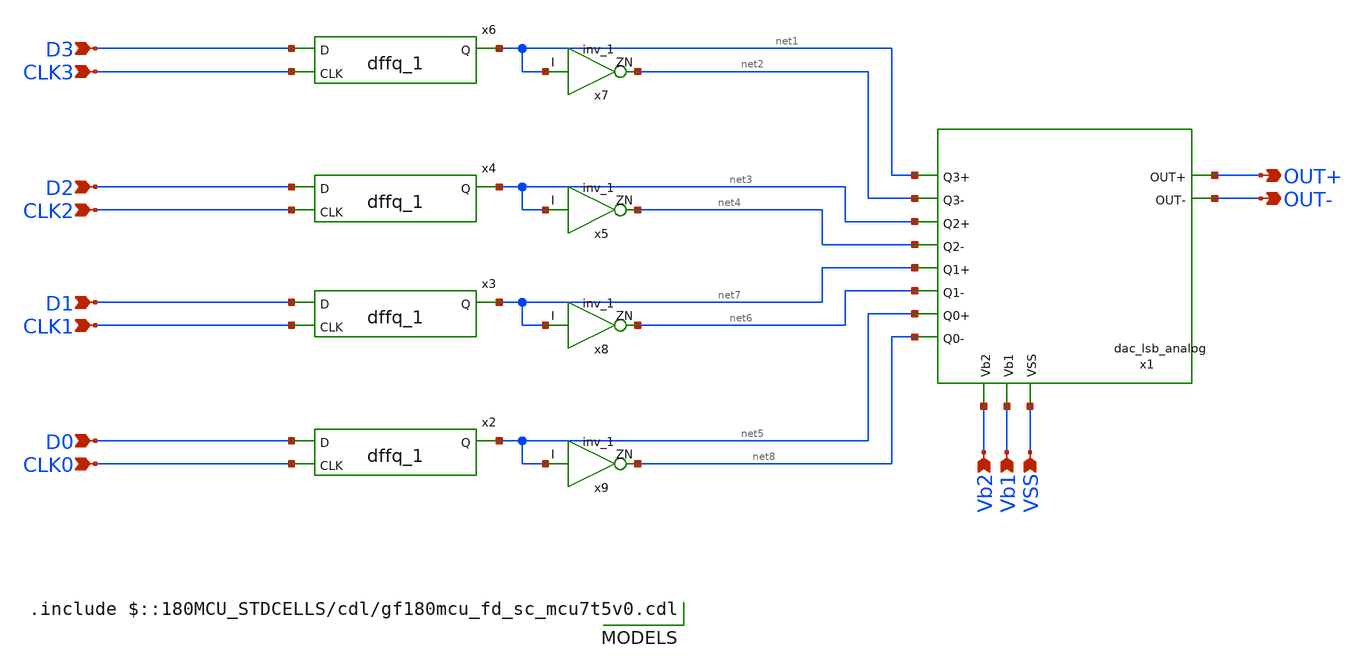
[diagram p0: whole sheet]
** sch_path: DAC/xschem/dac_lsb_matrix.sch
**.subckt dac_lsb_matrix D3 D2 D1 D0 CLK3 CLK2 CLK1 CLK0 VSS Vb2 Vb1 OUT+ OUT-
*.ipin D3
*.ipin D2
*.ipin D1
*.ipin D0
*.ipin CLK3
*.ipin CLK2
*.ipin CLK1
*.ipin CLK0
*.ipin VSS
*.ipin Vb2
*.ipin Vb1
*.opin OUT+
*.opin OUT-
x1 OUT+ OUT- net4 net1 net6 net3 net2 net7 net8 net5 Vb2 Vb1 VSS dac_lsb_analog
x6 D3 CLK3 net1 DVDD DVDD DVSS DVSS gf180mcu_fd_sc_mcu7t5v0__dffq_1
x7 net1 net2 DVDD DVDD DVSS DVSS gf180mcu_fd_sc_mcu7t5v0__inv_1
x4 D2 CLK2 net3 DVDD DVDD DVSS DVSS gf180mcu_fd_sc_mcu7t5v0__dffq_1
x5 net3 net4 DVDD DVDD DVSS DVSS gf180mcu_fd_sc_mcu7t5v0__inv_1
x3 D1 CLK1 net7 DVDD DVDD DVSS DVSS gf180mcu_fd_sc_mcu7t5v0__dffq_1
x8 net7 net6 DVDD DVDD DVSS DVSS gf180mcu_fd_sc_mcu7t5v0__inv_1
x2 D0 CLK0 net5 DVDD DVDD DVSS DVSS gf180mcu_fd_sc_mcu7t5v0__dffq_1
x9 net5 net8 DVDD DVDD DVSS DVSS gf180mcu_fd_sc_mcu7t5v0__inv_1
**** begin user architecture code

.include $::180MCU_STDCELLS/cdl/gf180mcu_fd_sc_mcu7t5v0.cdl

**** end user architecture code
**.ends

* expanding   symbol:  dac_lsb_analog.sym # of pins=13
** sym_path: DAC/xschem/dac_lsb_analog.sym
** sch_path: DAC/xschem/dac_lsb_analog.sch
.subckt dac_lsb_analog OUT+ OUT- Q2- Q3+ Q1- Q2+ Q3- Q1+ Q0- Q0+ Vb2 Vb1 VSS
*.ipin VSS
*.ipin Vb2
*.ipin Vb1
*.ipin Q3-
*.ipin Q3+
*.ipin Q2-
*.ipin Q2+
*.ipin Q1-
*.ipin Q1+
*.ipin Q0-
*.ipin Q0+
*.opin OUT+
*.opin OUT-
XM7 net1 Vb2 net2 VSS nfet_03v3 L=0.5u W=2u nf=2 ad='int((nf+1)/2) * W/nf * 0.18u' as='int((nf+2)/2) * W/nf * 0.18u'
+ pd='2*int((nf+1)/2) * (W/nf + 0.18u)' ps='2*int((nf+2)/2) * (W/nf + 0.18u)' nrd='0.18u / W' nrs='0.18u / W'
+ sa=0 sb=0 sd=0 m=1
XM8 net2 Vb1 VSS VSS nfet_03v3 L=0.5u W=2u nf=1 ad='int((nf+1)/2) * W/nf * 0.18u' as='int((nf+2)/2) * W/nf * 0.18u'
+ pd='2*int((nf+1)/2) * (W/nf + 0.18u)' ps='2*int((nf+2)/2) * (W/nf + 0.18u)' nrd='0.18u / W' nrs='0.18u / W'
+ sa=0 sb=0 sd=0 m=1
XM12 OUT+ Q0+ net1 VSS nfet_03v3 L=0.5u W=1u nf=1 ad='int((nf+1)/2) * W/nf * 0.18u' as='int((nf+2)/2) * W/nf * 0.18u'
+ pd='2*int((nf+1)/2) * (W/nf + 0.18u)' ps='2*int((nf+2)/2) * (W/nf + 0.18u)' nrd='0.18u / W' nrs='0.18u / W'
+ sa=0 sb=0 sd=0 m=1
XM13 OUT- Q0- net1 VSS nfet_03v3 L=0.5u W=1u nf=1 ad='int((nf+1)/2) * W/nf * 0.18u' as='int((nf+2)/2) * W/nf * 0.18u'
+ pd='2*int((nf+1)/2) * (W/nf + 0.18u)' ps='2*int((nf+2)/2) * (W/nf + 0.18u)' nrd='0.18u / W' nrs='0.18u / W'
+ sa=0 sb=0 sd=0 m=1
XM14 net3 Vb2 net4 VSS nfet_03v3 L=0.5u W=4u nf=4 ad='int((nf+1)/2) * W/nf * 0.18u' as='int((nf+2)/2) * W/nf * 0.18u'
+ pd='2*int((nf+1)/2) * (W/nf + 0.18u)' ps='2*int((nf+2)/2) * (W/nf + 0.18u)' nrd='0.18u / W' nrs='0.18u / W'
+ sa=0 sb=0 sd=0 m=1
XM15 net4 Vb1 VSS VSS nfet_03v3 L=0.5u W=4u nf=2 ad='int((nf+1)/2) * W/nf * 0.18u' as='int((nf+2)/2) * W/nf * 0.18u'
+ pd='2*int((nf+1)/2) * (W/nf + 0.18u)' ps='2*int((nf+2)/2) * (W/nf + 0.18u)' nrd='0.18u / W' nrs='0.18u / W'
+ sa=0 sb=0 sd=0 m=1
XM18 OUT+ Q1+ net3 VSS nfet_03v3 L=0.5u W=2u nf=2 ad='int((nf+1)/2) * W/nf * 0.18u' as='int((nf+2)/2) * W/nf * 0.18u'
+ pd='2*int((nf+1)/2) * (W/nf + 0.18u)' ps='2*int((nf+2)/2) * (W/nf + 0.18u)' nrd='0.18u / W' nrs='0.18u / W'
+ sa=0 sb=0 sd=0 m=1
XM19 OUT- Q1- net3 VSS nfet_03v3 L=0.5u W=2u nf=2 ad='int((nf+1)/2) * W/nf * 0.18u' as='int((nf+2)/2) * W/nf * 0.18u'
+ pd='2*int((nf+1)/2) * (W/nf + 0.18u)' ps='2*int((nf+2)/2) * (W/nf + 0.18u)' nrd='0.18u / W' nrs='0.18u / W'
+ sa=0 sb=0 sd=0 m=1
XM20 net5 Vb2 net6 VSS nfet_03v3 L=0.5u W=8u nf=8 ad='int((nf+1)/2) * W/nf * 0.18u' as='int((nf+2)/2) * W/nf * 0.18u'
+ pd='2*int((nf+1)/2) * (W/nf + 0.18u)' ps='2*int((nf+2)/2) * (W/nf + 0.18u)' nrd='0.18u / W' nrs='0.18u / W'
+ sa=0 sb=0 sd=0 m=1
XM21 net6 Vb1 VSS VSS nfet_03v3 L=0.5u W=8u nf=4 ad='int((nf+1)/2) * W/nf * 0.18u' as='int((nf+2)/2) * W/nf * 0.18u'
+ pd='2*int((nf+1)/2) * (W/nf + 0.18u)' ps='2*int((nf+2)/2) * (W/nf + 0.18u)' nrd='0.18u / W' nrs='0.18u / W'
+ sa=0 sb=0 sd=0 m=1
XM24 OUT+ Q2+ net5 VSS nfet_03v3 L=0.5u W=4u nf=4 ad='int((nf+1)/2) * W/nf * 0.18u' as='int((nf+2)/2) * W/nf * 0.18u'
+ pd='2*int((nf+1)/2) * (W/nf + 0.18u)' ps='2*int((nf+2)/2) * (W/nf + 0.18u)' nrd='0.18u / W' nrs='0.18u / W'
+ sa=0 sb=0 sd=0 m=1
XM25 OUT- Q2- net5 VSS nfet_03v3 L=0.5u W=4u nf=4 ad='int((nf+1)/2) * W/nf * 0.18u' as='int((nf+2)/2) * W/nf * 0.18u'
+ pd='2*int((nf+1)/2) * (W/nf + 0.18u)' ps='2*int((nf+2)/2) * (W/nf + 0.18u)' nrd='0.18u / W' nrs='0.18u / W'
+ sa=0 sb=0 sd=0 m=1
XM26 net7 Vb2 net8 VSS nfet_03v3 L=0.5u W=16u nf=16 ad='int((nf+1)/2) * W/nf * 0.18u' as='int((nf+2)/2) * W/nf * 0.18u'
+ pd='2*int((nf+1)/2) * (W/nf + 0.18u)' ps='2*int((nf+2)/2) * (W/nf + 0.18u)' nrd='0.18u / W' nrs='0.18u / W'
+ sa=0 sb=0 sd=0 m=1
XM27 net8 Vb1 VSS VSS nfet_03v3 L=0.5u W=16u nf=8 ad='int((nf+1)/2) * W/nf * 0.18u' as='int((nf+2)/2) * W/nf * 0.18u'
+ pd='2*int((nf+1)/2) * (W/nf + 0.18u)' ps='2*int((nf+2)/2) * (W/nf + 0.18u)' nrd='0.18u / W' nrs='0.18u / W'
+ sa=0 sb=0 sd=0 m=1
XM30 OUT+ Q3+ net7 VSS nfet_03v3 L=0.5u W=8u nf=8 ad='int((nf+1)/2) * W/nf * 0.18u' as='int((nf+2)/2) * W/nf * 0.18u'
+ pd='2*int((nf+1)/2) * (W/nf + 0.18u)' ps='2*int((nf+2)/2) * (W/nf + 0.18u)' nrd='0.18u / W' nrs='0.18u / W'
+ sa=0 sb=0 sd=0 m=1
XM31 OUT- Q3- net7 VSS nfet_03v3 L=0.5u W=8u nf=8 ad='int((nf+1)/2) * W/nf * 0.18u' as='int((nf+2)/2) * W/nf * 0.18u'
+ pd='2*int((nf+1)/2) * (W/nf + 0.18u)' ps='2*int((nf+2)/2) * (W/nf + 0.18u)' nrd='0.18u / W' nrs='0.18u / W'
+ sa=0 sb=0 sd=0 m=1
.ends

.end
